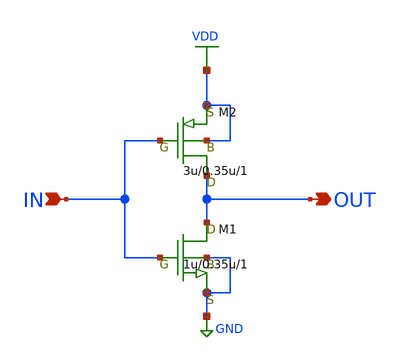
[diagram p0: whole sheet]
** sch_path: LR_hokari/LR_Work2/Clocked_Comparator_Xschem/INVERTER.sch
**.subckt INVERTER IN OUT
*.ipin IN
*.opin OUT
M1 OUT IN GND GND nch w=1u l=0.35u as=2.8p ps=5.5u ad=2..8p pd=5.5u m=1
M2 OUT IN VDD VDD pch w=3u l=0.35u as=5.6p ps=9u ad=5.6p pd=9u m=1
**.ends
.GLOBAL VDD
.GLOBAL GND
.end
